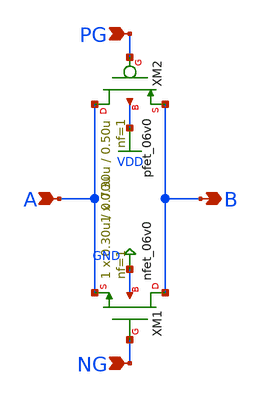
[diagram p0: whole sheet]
** sch_path: tmg.sch
**.subckt tmg B A PG NG
*.opin B
*.ipin A
*.ipin PG
*.ipin NG
XM1 B NG A GND nfet_06v0 L=0.70u W=0.30u nf=1 ad='int((nf+1)/2) * W/nf * 0.18u' as='int((nf+2)/2) * W/nf * 0.18u'
+ pd='2*int((nf+1)/2) * (W/nf + 0.18u)' ps='2*int((nf+2)/2) * (W/nf + 0.18u)' nrd='0.18u / W' nrs='0.18u / W'
+ sa=0 sb=0 sd=0 m=1
XM2 A PG B VDD pfet_06v0 L=0.50u W=0.30u nf=1 ad='int((nf+1)/2) * W/nf * 0.18u' as='int((nf+2)/2) * W/nf * 0.18u'
+ pd='2*int((nf+1)/2) * (W/nf + 0.18u)' ps='2*int((nf+2)/2) * (W/nf + 0.18u)' nrd='0.18u / W' nrs='0.18u / W'
+ sa=0 sb=0 sd=0 m=1
**.ends
.GLOBAL GND
.GLOBAL VDD
.end
